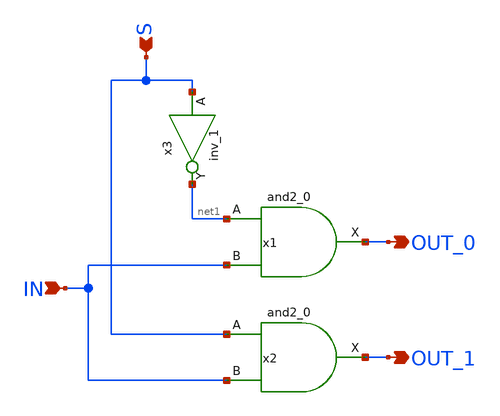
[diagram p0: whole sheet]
** sch_path: demux2.sch
**.subckt demux2 S OUT_0 IN OUT_1
*.ipin S
*.opin OUT_0
*.ipin IN
*.opin OUT_1
x1 net1 IN VSS VSS VDD VDD OUT_0 sky130_fd_sc_hd__and2_0
x2 S IN VSS VSS VDD VDD OUT_1 sky130_fd_sc_hd__and2_0
x3 S VSS VSS VDD VDD net1 sky130_fd_sc_hd__inv_1
**.ends
.end
